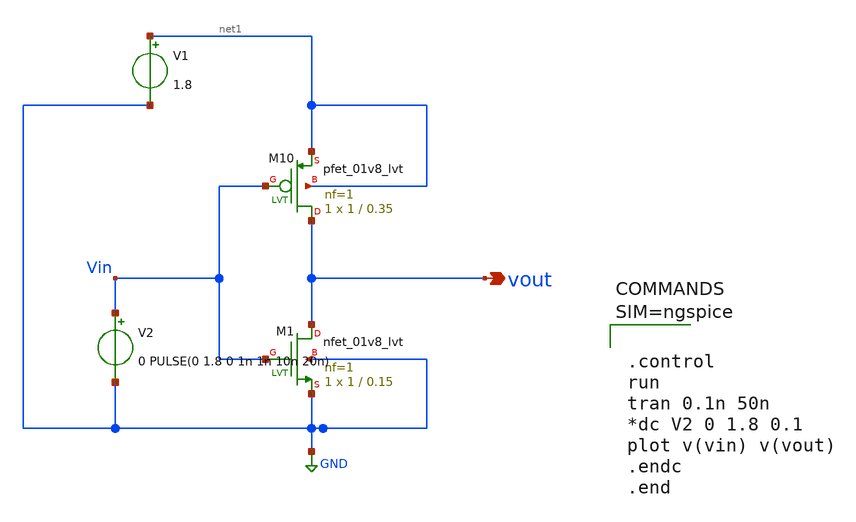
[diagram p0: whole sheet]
** sch_path: xschem/untitled-6.sch
**.subckt untitled-6 vout
*.opin vout
XM1 vout Vin GND GND sky130_fd_pr__nfet_01v8_lvt L=0.15 W=1 nf=1 ad='int((1 + 1)/2) * 1 / 1 * 0.29' as='int((1 + 2)/2) * 1 / 1 * 0.29'
+ pd='2*int((1 + 1)/2) * (1 / 1 + 0.29)' ps='2*int((1 + 2)/2) * (1 / 1 + 0.29)' nrd='0.29 / 1 ' nrs='0.29 / 1 '
+ sa=0 sb=0 sd=0 mult=1 m=1
XM10 vout Vin net1 net1 sky130_fd_pr__pfet_01v8_lvt L=0.35 W=1 nf=1 ad='int((1 + 1)/2) * 1 / 1 * 0.29'
+ as='int((1 + 2)/2) * 1 / 1 * 0.29' pd='2*int((1 + 1)/2) * (1 / 1 + 0.29)' ps='2*int((1 + 2)/2) * (1 / 1 + 0.29)'
+ nrd='0.29 / 1 ' nrs='0.29 / 1 ' sa=0 sb=0 sd=0 mult=1 m=1
V1 net1 GND 1.8
V2 Vin GND 0 PULSE(0 1.8 0 1n 1n 10n 20n)
**** begin user architecture code

** opencircuitdesign pdks install
.lib $::SKYWATER_MODELS/sky130.lib.spice tt




.control
run
tran 0.1n 50n
*dc V2 0 1.8 0.1
plot v(vin) v(vout)
.endc
.end


**** end user architecture code
**.ends
.GLOBAL GND
.end
